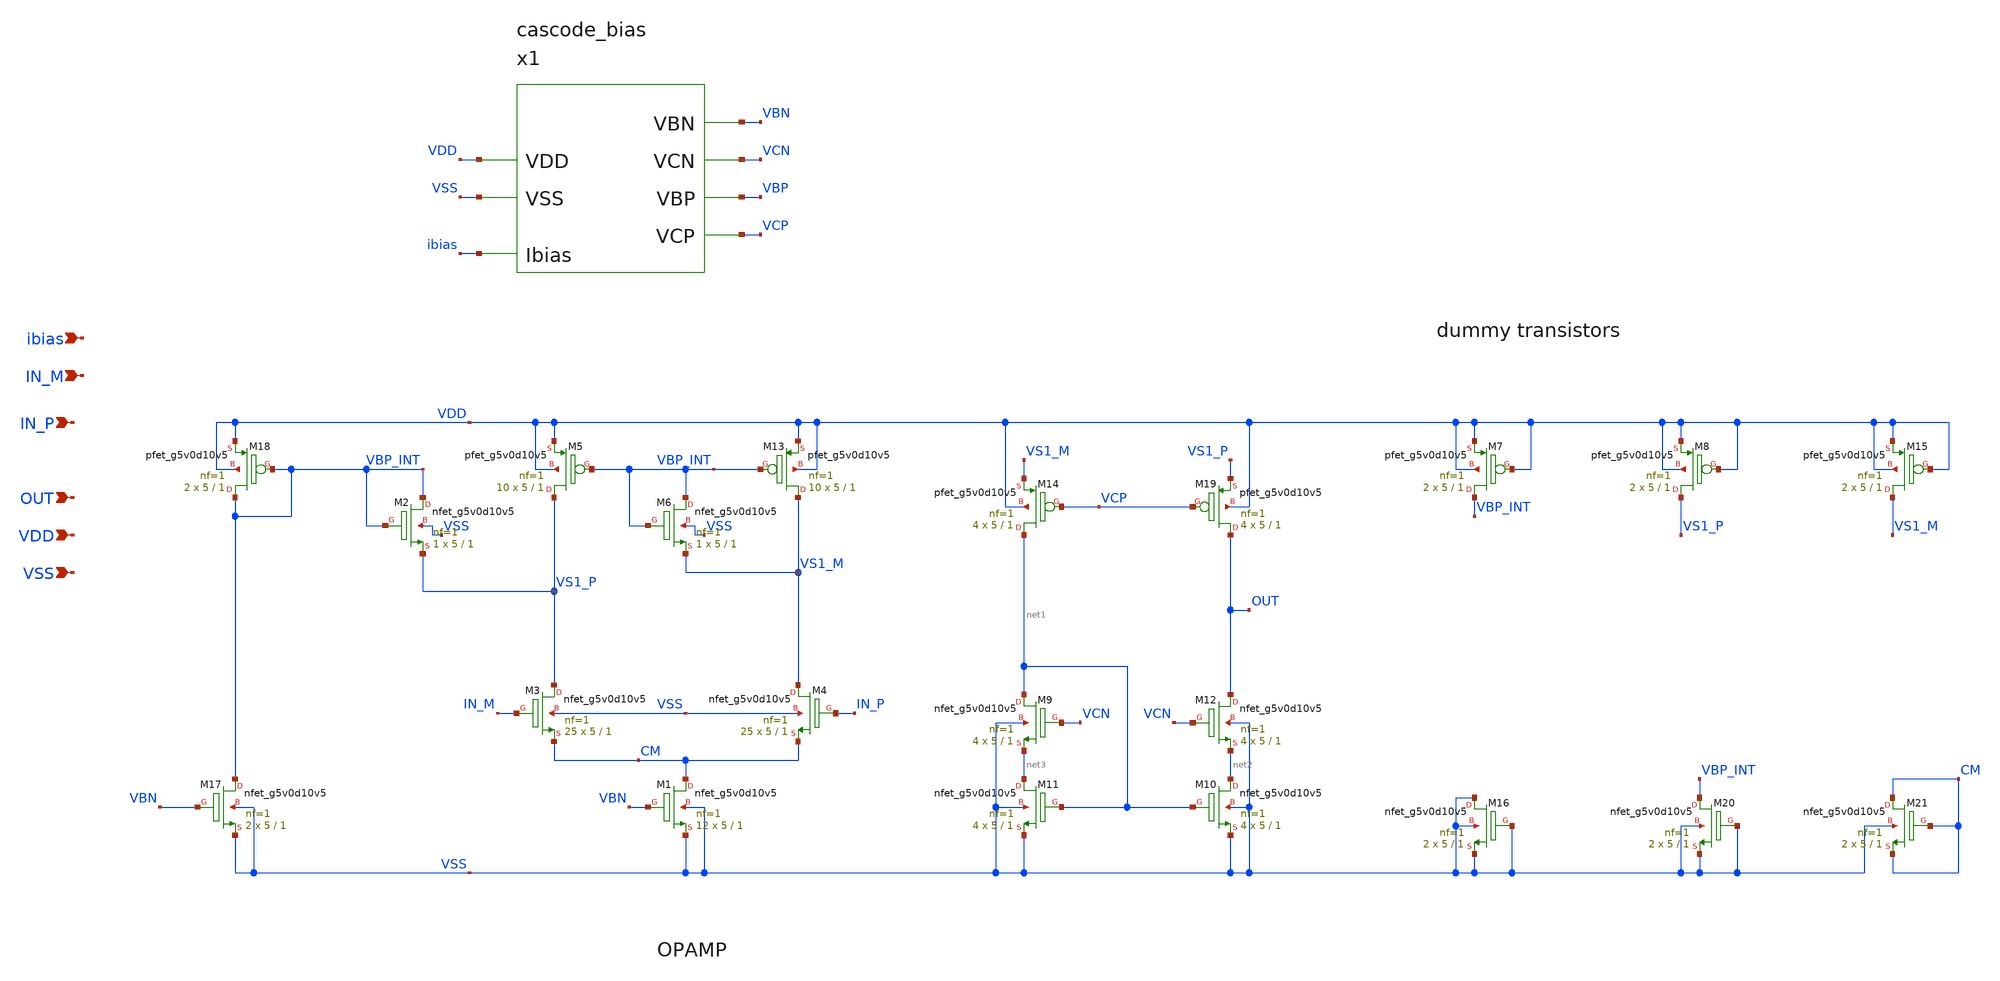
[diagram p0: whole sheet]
** sch_path: images/iic-osic-tools/addons/examples/open-pmic/design/folded-cascode-n-in/folded_cascode_n_in.sch
**.subckt folded_cascode_n_in IN_M IN_P OUT VDD VSS ibias
*.ipin IN_M
*.ipin IN_P
*.ipin OUT
*.ipin VDD
*.ipin VSS
*.ipin ibias
XM1 CM VBN VSS VSS sky130_fd_pr__nfet_g5v0d10v5 L=1 W=5 nf=1 ad='int((nf+1)/2) * W/nf * 0.29' as='int((nf+2)/2) * W/nf * 0.29'
+ pd='2*int((nf+1)/2) * (W/nf + 0.29)' ps='2*int((nf+2)/2) * (W/nf + 0.29)' nrd='0.29 / W' nrs='0.29 / W'
+ sa=0 sb=0 sd=0 mult=12 m=12
XM12 OUT VCN net2 VSS sky130_fd_pr__nfet_g5v0d10v5 L=1 W=5 nf=1 ad='int((nf+1)/2) * W/nf * 0.29' as='int((nf+2)/2) * W/nf * 0.29'
+ pd='2*int((nf+1)/2) * (W/nf + 0.29)' ps='2*int((nf+2)/2) * (W/nf + 0.29)' nrd='0.29 / W' nrs='0.29 / W'
+ sa=0 sb=0 sd=0 mult=4 m=4
XM4 VS1_M IN_P CM VSS sky130_fd_pr__nfet_g5v0d10v5 L=1 W=5 nf=1 ad='int((nf+1)/2) * W/nf * 0.29' as='int((nf+2)/2) * W/nf * 0.29'
+ pd='2*int((nf+1)/2) * (W/nf + 0.29)' ps='2*int((nf+2)/2) * (W/nf + 0.29)' nrd='0.29 / W' nrs='0.29 / W'
+ sa=0 sb=0 sd=0 mult=25 m=25
XM9 net1 VCN net3 VSS sky130_fd_pr__nfet_g5v0d10v5 L=1 W=5 nf=1 ad='int((nf+1)/2) * W/nf * 0.29' as='int((nf+2)/2) * W/nf * 0.29'
+ pd='2*int((nf+1)/2) * (W/nf + 0.29)' ps='2*int((nf+2)/2) * (W/nf + 0.29)' nrd='0.29 / W' nrs='0.29 / W'
+ sa=0 sb=0 sd=0 mult=4 m=4
XM10 net2 net1 VSS VSS sky130_fd_pr__nfet_g5v0d10v5 L=1 W=5 nf=1 ad='int((nf+1)/2) * W/nf * 0.29' as='int((nf+2)/2) * W/nf * 0.29'
+ pd='2*int((nf+1)/2) * (W/nf + 0.29)' ps='2*int((nf+2)/2) * (W/nf + 0.29)' nrd='0.29 / W' nrs='0.29 / W'
+ sa=0 sb=0 sd=0 mult=4 m=4
XM11 net3 net1 VSS VSS sky130_fd_pr__nfet_g5v0d10v5 L=1 W=5 nf=1 ad='int((nf+1)/2) * W/nf * 0.29' as='int((nf+2)/2) * W/nf * 0.29'
+ pd='2*int((nf+1)/2) * (W/nf + 0.29)' ps='2*int((nf+2)/2) * (W/nf + 0.29)' nrd='0.29 / W' nrs='0.29 / W'
+ sa=0 sb=0 sd=0 mult=4 m=4
XM3 VS1_P IN_M CM VSS sky130_fd_pr__nfet_g5v0d10v5 L=1 W=5 nf=1 ad='int((nf+1)/2) * W/nf * 0.29' as='int((nf+2)/2) * W/nf * 0.29'
+ pd='2*int((nf+1)/2) * (W/nf + 0.29)' ps='2*int((nf+2)/2) * (W/nf + 0.29)' nrd='0.29 / W' nrs='0.29 / W'
+ sa=0 sb=0 sd=0 mult=25 m=25
XM5 VS1_P VBP_INT VDD VDD sky130_fd_pr__pfet_g5v0d10v5 L=1 W=5 nf=1 ad='int((nf+1)/2) * W/nf * 0.29'
+ as='int((nf+2)/2) * W/nf * 0.29' pd='2*int((nf+1)/2) * (W/nf + 0.29)' ps='2*int((nf+2)/2) * (W/nf + 0.29)'
+ nrd='0.29 / W' nrs='0.29 / W' sa=0 sb=0 sd=0 mult=10 m=10
XM13 VS1_M VBP_INT VDD VDD sky130_fd_pr__pfet_g5v0d10v5 L=1 W=5 nf=1 ad='int((nf+1)/2) * W/nf * 0.29'
+ as='int((nf+2)/2) * W/nf * 0.29' pd='2*int((nf+1)/2) * (W/nf + 0.29)' ps='2*int((nf+2)/2) * (W/nf + 0.29)'
+ nrd='0.29 / W' nrs='0.29 / W' sa=0 sb=0 sd=0 mult=10 m=10
XM17 VBP_INT VBN VSS VSS sky130_fd_pr__nfet_g5v0d10v5 L=1 W=5 nf=1 ad='int((nf+1)/2) * W/nf * 0.29' as='int((nf+2)/2) * W/nf * 0.29'
+ pd='2*int((nf+1)/2) * (W/nf + 0.29)' ps='2*int((nf+2)/2) * (W/nf + 0.29)' nrd='0.29 / W' nrs='0.29 / W'
+ sa=0 sb=0 sd=0 mult=2 m=2
XM18 VBP_INT VBP_INT VDD VDD sky130_fd_pr__pfet_g5v0d10v5 L=1 W=5 nf=1 ad='int((nf+1)/2) * W/nf * 0.29'
+ as='int((nf+2)/2) * W/nf * 0.29' pd='2*int((nf+1)/2) * (W/nf + 0.29)' ps='2*int((nf+2)/2) * (W/nf + 0.29)'
+ nrd='0.29 / W' nrs='0.29 / W' sa=0 sb=0 sd=0 mult=2 m=2
XM14 net1 VCP VS1_M VDD sky130_fd_pr__pfet_g5v0d10v5 L=1 W=5 nf=1 ad='int((nf+1)/2) * W/nf * 0.29' as='int((nf+2)/2) * W/nf * 0.29'
+ pd='2*int((nf+1)/2) * (W/nf + 0.29)' ps='2*int((nf+2)/2) * (W/nf + 0.29)' nrd='0.29 / W' nrs='0.29 / W'
+ sa=0 sb=0 sd=0 mult=4 m=4
XM19 OUT VCP VS1_P VDD sky130_fd_pr__pfet_g5v0d10v5 L=1 W=5 nf=1 ad='int((nf+1)/2) * W/nf * 0.29' as='int((nf+2)/2) * W/nf * 0.29'
+ pd='2*int((nf+1)/2) * (W/nf + 0.29)' ps='2*int((nf+2)/2) * (W/nf + 0.29)' nrd='0.29 / W' nrs='0.29 / W'
+ sa=0 sb=0 sd=0 mult=4 m=4
XM2 VBP_INT VBP_INT VS1_P VSS sky130_fd_pr__nfet_g5v0d10v5 L=1 W=5 nf=1 ad='int((nf+1)/2) * W/nf * 0.29'
+ as='int((nf+2)/2) * W/nf * 0.29' pd='2*int((nf+1)/2) * (W/nf + 0.29)' ps='2*int((nf+2)/2) * (W/nf + 0.29)'
+ nrd='0.29 / W' nrs='0.29 / W' sa=0 sb=0 sd=0 mult=1 m=1
XM6 VBP_INT VBP_INT VS1_M VSS sky130_fd_pr__nfet_g5v0d10v5 L=1 W=5 nf=1 ad='int((nf+1)/2) * W/nf * 0.29'
+ as='int((nf+2)/2) * W/nf * 0.29' pd='2*int((nf+1)/2) * (W/nf + 0.29)' ps='2*int((nf+2)/2) * (W/nf + 0.29)'
+ nrd='0.29 / W' nrs='0.29 / W' sa=0 sb=0 sd=0 mult=1 m=1
x1 VBN VCN VBP VCP VDD VSS ibias cascode_bias
XM7 VBP_INT VDD VDD VDD sky130_fd_pr__pfet_g5v0d10v5 L=1 W=5 nf=1 ad='int((nf+1)/2) * W/nf * 0.29' as='int((nf+2)/2) * W/nf * 0.29'
+ pd='2*int((nf+1)/2) * (W/nf + 0.29)' ps='2*int((nf+2)/2) * (W/nf + 0.29)' nrd='0.29 / W' nrs='0.29 / W'
+ sa=0 sb=0 sd=0 mult=2 m=2
XM8 VS1_P VDD VDD VDD sky130_fd_pr__pfet_g5v0d10v5 L=1 W=5 nf=1 ad='int((nf+1)/2) * W/nf * 0.29' as='int((nf+2)/2) * W/nf * 0.29'
+ pd='2*int((nf+1)/2) * (W/nf + 0.29)' ps='2*int((nf+2)/2) * (W/nf + 0.29)' nrd='0.29 / W' nrs='0.29 / W'
+ sa=0 sb=0 sd=0 mult=2 m=2
XM15 VS1_M VDD VDD VDD sky130_fd_pr__pfet_g5v0d10v5 L=1 W=5 nf=1 ad='int((nf+1)/2) * W/nf * 0.29' as='int((nf+2)/2) * W/nf * 0.29'
+ pd='2*int((nf+1)/2) * (W/nf + 0.29)' ps='2*int((nf+2)/2) * (W/nf + 0.29)' nrd='0.29 / W' nrs='0.29 / W'
+ sa=0 sb=0 sd=0 mult=2 m=2
XM16 VSS VSS VSS VSS sky130_fd_pr__nfet_g5v0d10v5 L=1 W=5 nf=1 ad='int((nf+1)/2) * W/nf * 0.29' as='int((nf+2)/2) * W/nf * 0.29'
+ pd='2*int((nf+1)/2) * (W/nf + 0.29)' ps='2*int((nf+2)/2) * (W/nf + 0.29)' nrd='0.29 / W' nrs='0.29 / W'
+ sa=0 sb=0 sd=0 mult=2 m=2
XM20 VBP_INT VSS VSS VSS sky130_fd_pr__nfet_g5v0d10v5 L=1 W=5 nf=1 ad='int((nf+1)/2) * W/nf * 0.29' as='int((nf+2)/2) * W/nf * 0.29'
+ pd='2*int((nf+1)/2) * (W/nf + 0.29)' ps='2*int((nf+2)/2) * (W/nf + 0.29)' nrd='0.29 / W' nrs='0.29 / W'
+ sa=0 sb=0 sd=0 mult=2 m=2
XM21 CM CM CM VSS sky130_fd_pr__nfet_g5v0d10v5 L=1 W=5 nf=1 ad='int((nf+1)/2) * W/nf * 0.29' as='int((nf+2)/2) * W/nf * 0.29'
+ pd='2*int((nf+1)/2) * (W/nf + 0.29)' ps='2*int((nf+2)/2) * (W/nf + 0.29)' nrd='0.29 / W' nrs='0.29 / W'
+ sa=0 sb=0 sd=0 mult=2 m=2
**.ends
.end
